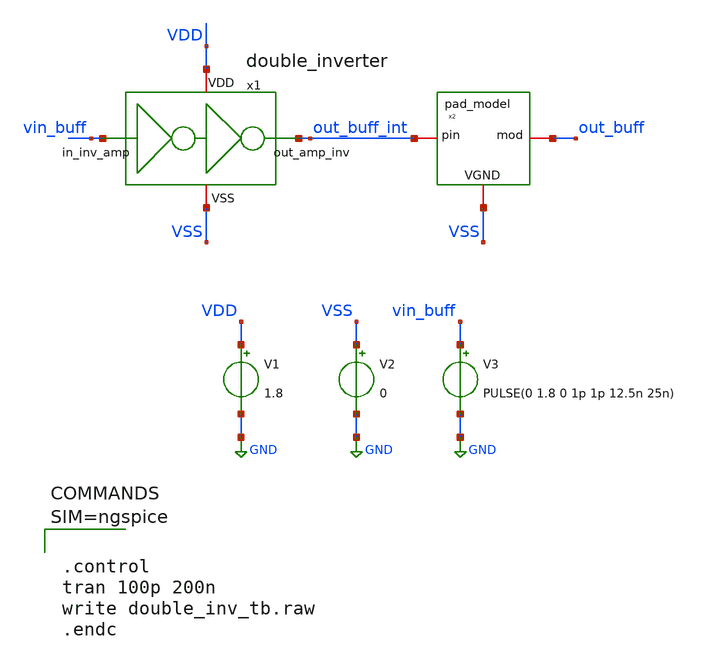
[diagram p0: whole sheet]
** sch_path: xschem/double_inv_tb.sch
**.subckt double_inv_tb
V1 VDD GND 1.8
V2 VSS GND 0
x1 VDD VSS out_buff_int vin_buff double_inverter
x2 VSS out_buff_int out_buff pad_model
V3 vin_buff GND PULSE(0 1.8 0 1p 1p 12.5n 25n)
**** begin user architecture code

** opencircuitdesign pdks install
.lib $::SKYWATER_MODELS/sky130.lib.spice tt





.control
tran 100p 200n
write double_inv_tb.raw
.endc



**** end user architecture code
**.ends
.GLOBAL GND
.end
